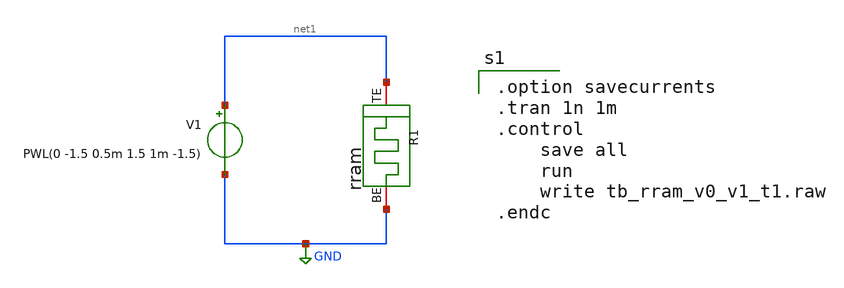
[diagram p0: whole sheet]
** sch_path: designs/tb_memristor/tb_rram_v0_v1_t1.sch
**.subckt tb_rram_v0_v1_t1
V1 net1 GND PWL(0 -1.5 0.5m 1.5 1m -1.5)
.save i(v1)
R1 net1 GND rram
**** begin user architecture code

.option savecurrents
.tran 1n 1m
.control
	save all
	run
	write tb_rram_v0_v1_t1.raw
.endc


.subckt rram BE TE
N1 BE TE rram_model
.model rram_model rram_va
.ends rram

.control
pre_osdi /foss/designs/spike_130/designs/memristors/rram_v0/rram.osdi
.endc

**** end user architecture code
**.ends
.GLOBAL GND
.end
